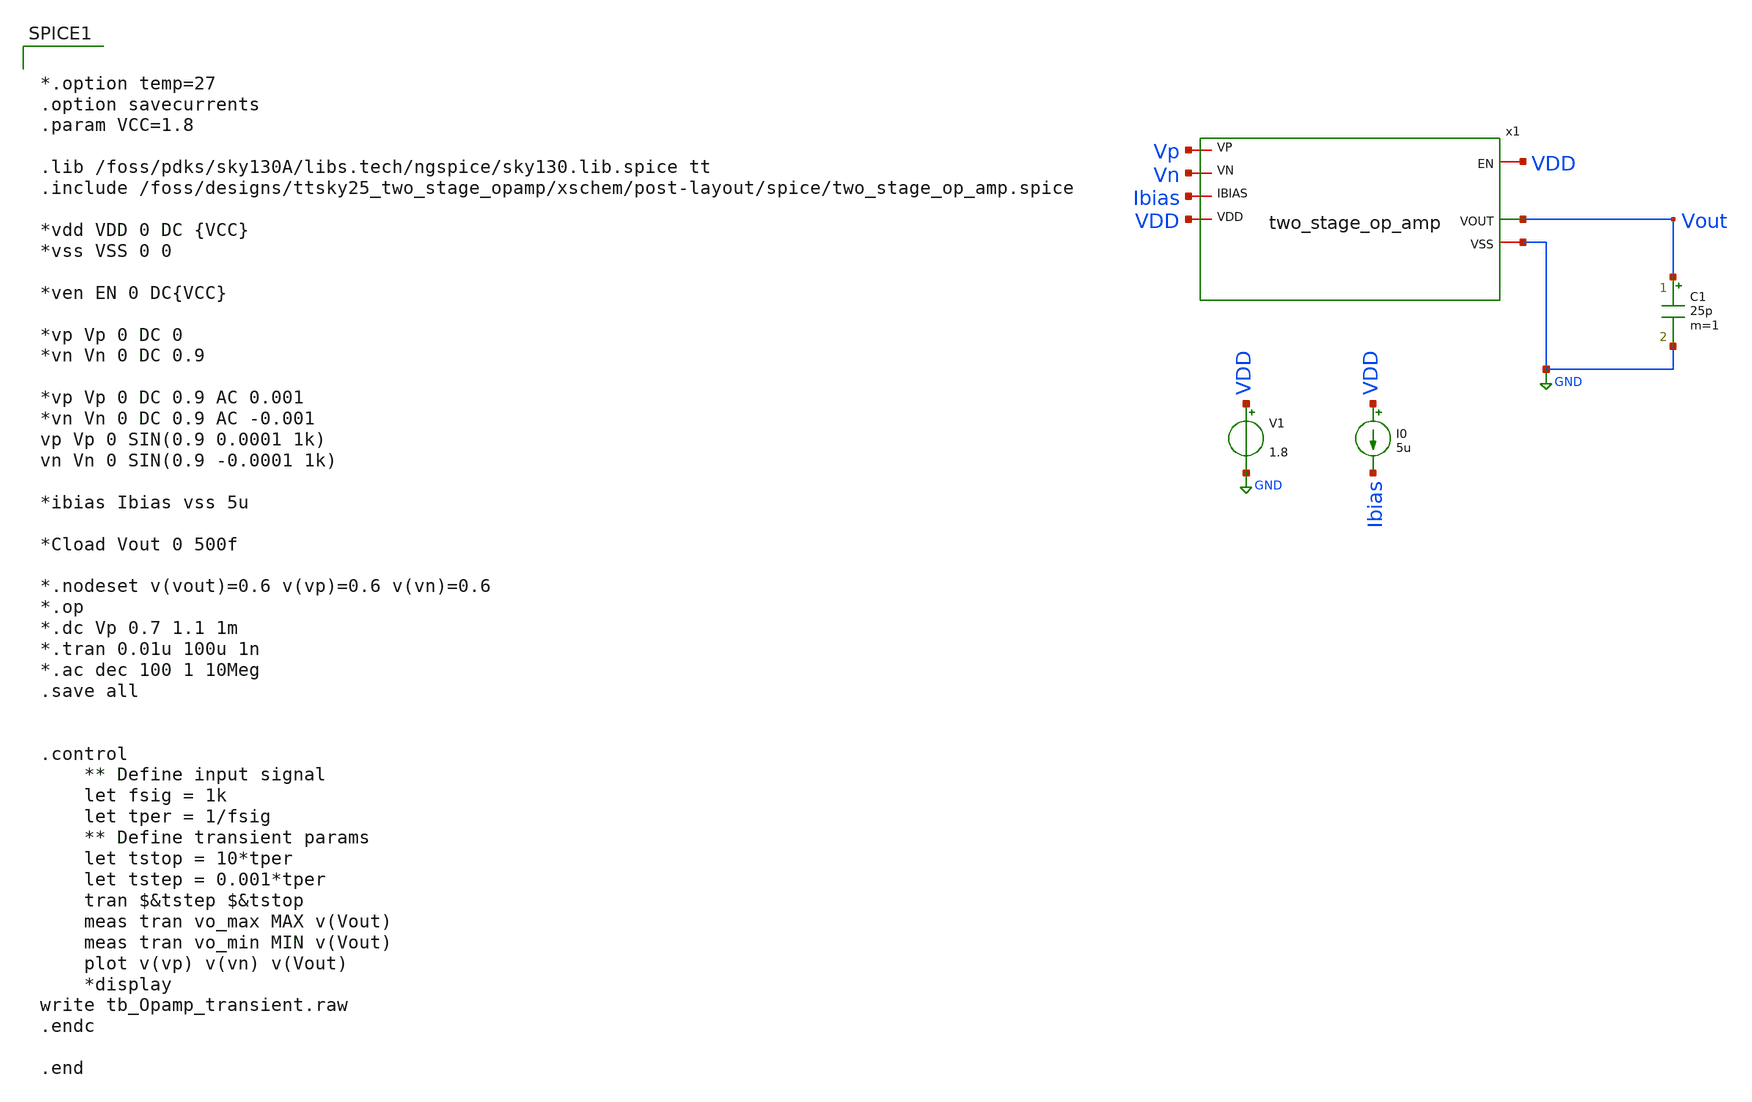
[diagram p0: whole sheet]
** sch_path: xschem/post-layout/testbenches/tb_Opamp_transient.sch
**.subckt tb_Opamp_transient
V1 VDD GND 1.8
I0 VDD Ibias 5u
C1 Vout GND 25p m=1
x1 VDD GND Ibias Vout Vp Vn VDD two_stage_op_amp
**** begin user architecture code


*.option temp=27
.option savecurrents
.param VCC=1.8

.lib /foss/pdks/sky130A/libs.tech/ngspice/sky130.lib.spice tt
.include /foss/designs/ttsky25_two_stage_opamp/xschem/post-layout/spice/two_stage_op_amp.spice

*vdd VDD 0 DC {VCC}
*vss VSS 0 0

*ven EN 0 DC{VCC}

*vp Vp 0 DC 0
*vn Vn 0 DC 0.9

*vp Vp 0 DC 0.9 AC 0.001
*vn Vn 0 DC 0.9 AC -0.001
vp Vp 0 SIN(0.9 0.0001 1k)
vn Vn 0 SIN(0.9 -0.0001 1k)

*ibias Ibias vss 5u

*Cload Vout 0 500f

*.nodeset v(vout)=0.6 v(vp)=0.6 v(vn)=0.6
*.op
*.dc Vp 0.7 1.1 1m
*.tran 0.01u 100u 1n
*.ac dec 100 1 10Meg
.save all


.control
	** Define input signal
	let fsig = 1k
	let tper = 1/fsig
	** Define transient params
	let tstop = 10*tper
	let tstep = 0.001*tper
	tran $&tstep $&tstop
	meas tran vo_max MAX v(Vout)
	meas tran vo_min MIN v(Vout)
	plot v(vp) v(vn) v(Vout)
	*display
write tb_Opamp_transient.raw
.endc

.end


**** end user architecture code
**.ends
.GLOBAL GND
.end
